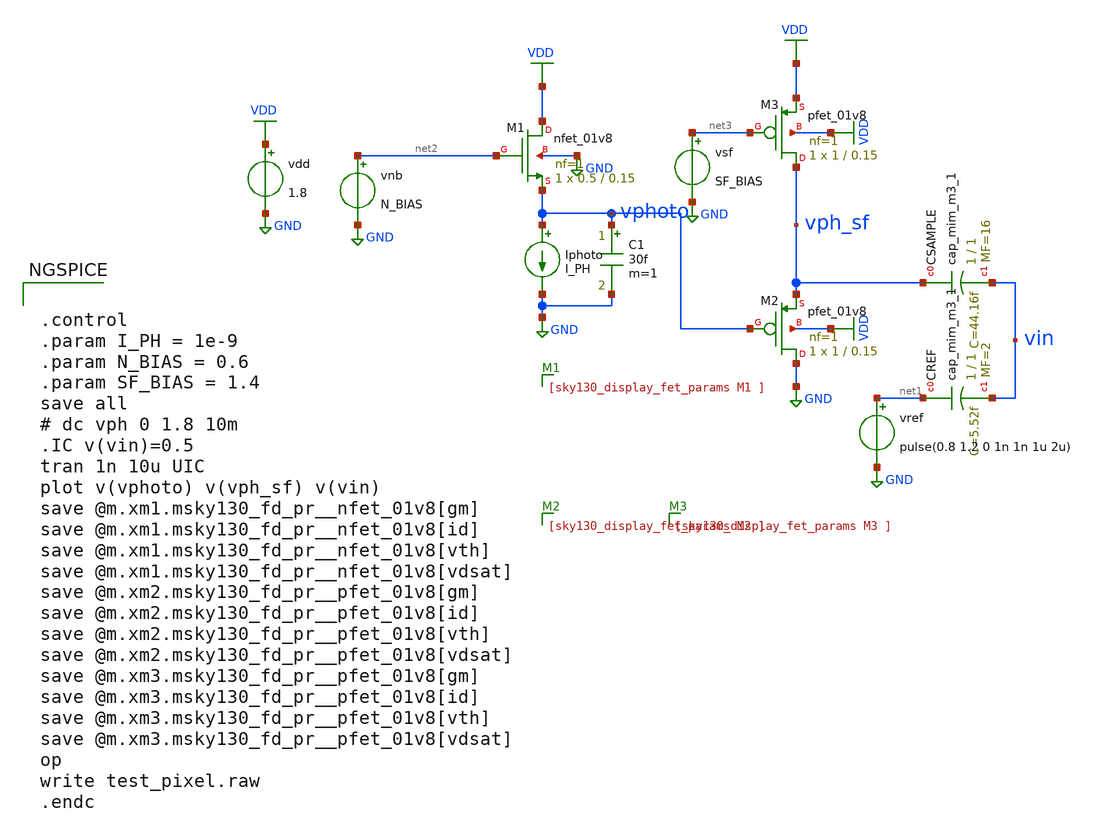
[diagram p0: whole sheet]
** sch_path: analog/klayout/production/final_merge_20260923/testbenches/cace/analog/xschem/test_pixel.sch
**.subckt test_pixel
vdd VDD GND 1.8
.save i(vdd)
XCSAMPLE vph_sf vin sky130_fd_pr__cap_mim_m3_1 W=1 L=1 MF=16 m=16
XCREF net1 vin sky130_fd_pr__cap_mim_m3_1 W=1 L=1 MF=2 m=2
C1 vphoto GND 30f m=1
XM1 VDD net2 vphoto GND sky130_fd_pr__nfet_01v8 L=0.15 W=0.5 nf=1 ad='int((1 + 1)/2) * 0.5 / 1 * 0.29'
+ as='int((1 + 2)/2) * 0.5 / 1 * 0.29' pd='2*int((1 + 1)/2) * (0.5 / 1 + 0.29)' ps='2*int((1 + 2)/2) * (0.5 / 1 + 0.29)'
+ nrd='0.29 / 0.5 ' nrs='0.29 / 0.5 ' sa=0 sb=0 sd=0 mult=1 m=1
vnb net2 GND N_BIAS
vsf net3 GND SF_BIAS
vref net1 GND pulse(0.8 1.2 0 1n 1n 1u 2u)
Iphoto vphoto GND I_PH
XM2 GND vphoto vph_sf VDD sky130_fd_pr__pfet_01v8 L=0.15 W=1 nf=1 ad='int((1 + 1)/2) * 1 / 1 * 0.29'
+ as='int((1 + 2)/2) * 1 / 1 * 0.29' pd='2*int((1 + 1)/2) * (1 / 1 + 0.29)' ps='2*int((1 + 2)/2) * (1 / 1 + 0.29)'
+ nrd='0.29 / 1 ' nrs='0.29 / 1 ' sa=0 sb=0 sd=0 mult=1 m=1
XM3 vph_sf net3 VDD VDD sky130_fd_pr__pfet_01v8 L=0.15 W=1 nf=1 ad='int((1 + 1)/2) * 1 / 1 * 0.29' as='int((1 + 2)/2) * 1 / 1 * 0.29'
+ pd='2*int((1 + 1)/2) * (1 / 1 + 0.29)' ps='2*int((1 + 2)/2) * (1 / 1 + 0.29)' nrd='0.29 / 1 ' nrs='0.29 / 1 '
+ sa=0 sb=0 sd=0 mult=1 m=1
**** begin user architecture code

** opencircuitdesign pdks install
.lib $::SKYWATER_MODELS/sky130.lib.spice tt



.control
.param I_PH = 1e-9
.param N_BIAS = 0.6
.param SF_BIAS = 1.4
save all
# dc vph 0 1.8 10m
.IC v(vin)=0.5
tran 1n 10u UIC
plot v(vphoto) v(vph_sf) v(vin)
save @m.xm1.msky130_fd_pr__nfet_01v8[gm]
save @m.xm1.msky130_fd_pr__nfet_01v8[id]
save @m.xm1.msky130_fd_pr__nfet_01v8[vth]
save @m.xm1.msky130_fd_pr__nfet_01v8[vdsat]
save @m.xm2.msky130_fd_pr__pfet_01v8[gm]
save @m.xm2.msky130_fd_pr__pfet_01v8[id]
save @m.xm2.msky130_fd_pr__pfet_01v8[vth]
save @m.xm2.msky130_fd_pr__pfet_01v8[vdsat]
save @m.xm3.msky130_fd_pr__pfet_01v8[gm]
save @m.xm3.msky130_fd_pr__pfet_01v8[id]
save @m.xm3.msky130_fd_pr__pfet_01v8[vth]
save @m.xm3.msky130_fd_pr__pfet_01v8[vdsat]
op
write test_pixel.raw
.endc


**** end user architecture code
**.ends
.GLOBAL VDD
.GLOBAL GND
.end
